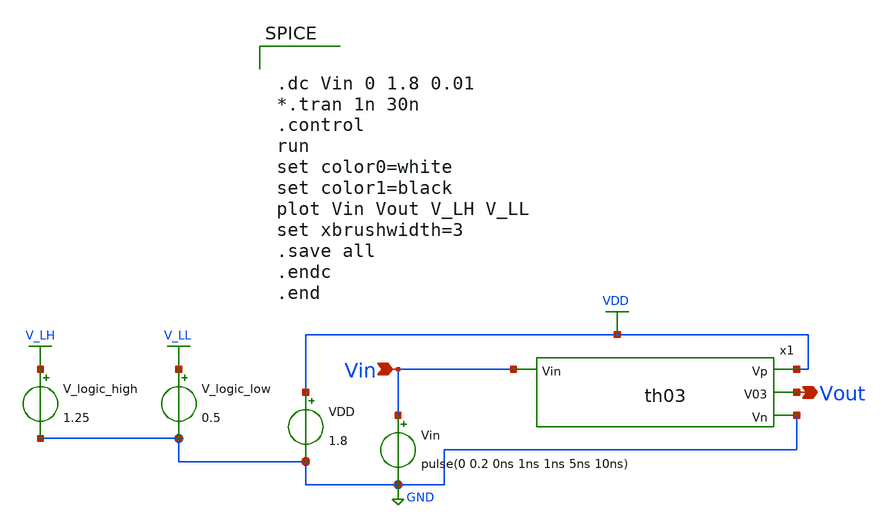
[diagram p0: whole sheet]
** sch_path: xschem/Vth_sch/Pre_layout/th03.sch
**.subckt th03 Vin Vout
*.ipin Vin
*.opin Vout
VDD VDD GND 1.8
Vin Vin GND pulse(0 0.2 0ns 1ns 1ns 5ns 10ns)
V_logic_high V_LH GND 1.25
V_logic_low V_LL GND 0.5
x1 VDD Vout Vin GND th03
**** begin user architecture code


.lib /usr/local/share/pdk/sky130A/libs.tech/ngspice/sky130.lib.spice tt

.save all





.dc Vin 0 1.8 0.01
*.tran 1n 30n
.control
run
set color0=white
set color1=black
plot Vin Vout V_LH V_LL
set xbrushwidth=3
.save all
.endc
.end


**** end user architecture code
**.ends

* expanding   symbol:  /home/exotic/Desktop/ASIC_ADC/xschem/Vth_sch/Symbol/th03.sym # of pins=4
** sym_path: xschem/Vth_sch/Symbol/th03.sym
** sch_path: xschem/Vth_sch/Symbol/th03.sch
.subckt th03 Vp V03 Vin Vn
*.opin Vn
*.opin Vp
*.ipin Vin
*.opin V03
XM3 V03 net1 Vp Vp sky130_fd_pr__pfet_01v8 L=0.156 W=1.0 nf=1 ad='int((nf+1)/2) * W/nf * 0.29' as='int((nf+2)/2) * W/nf * 0.29'
+ pd='2*int((nf+1)/2) * (W/nf + 0.29)' ps='2*int((nf+2)/2) * (W/nf + 0.29)' nrd='0.29 / W' nrs='0.29 / W'
+ sa=0 sb=0 sd=0 mult=1 m=1
XM4 V03 net1 Vn Vn sky130_fd_pr__nfet_01v8 L=1.5 W=0.40 nf=1 ad='int((nf+1)/2) * W/nf * 0.29' as='int((nf+2)/2) * W/nf * 0.29'
+ pd='2*int((nf+1)/2) * (W/nf + 0.29)' ps='2*int((nf+2)/2) * (W/nf + 0.29)' nrd='0.29 / W' nrs='0.29 / W'
+ sa=0 sb=0 sd=0 mult=1 m=1
XM1 net1 Vin net2 Vp sky130_fd_pr__pfet_01v8 L=1.36 W=0.44 nf=1 ad='int((nf+1)/2) * W/nf * 0.29' as='int((nf+2)/2) * W/nf * 0.29'
+ pd='2*int((nf+1)/2) * (W/nf + 0.29)' ps='2*int((nf+2)/2) * (W/nf + 0.29)' nrd='0.29 / W' nrs='0.29 / W'
+ sa=0 sb=0 sd=0 mult=1 m=1
XM0 net1 Vin Vn Vn sky130_fd_pr__nfet_01v8 L=0.153 W=1.1 nf=1 ad='int((nf+1)/2) * W/nf * 0.29' as='int((nf+2)/2) * W/nf * 0.29'
+ pd='2*int((nf+1)/2) * (W/nf + 0.29)' ps='2*int((nf+2)/2) * (W/nf + 0.29)' nrd='0.29 / W' nrs='0.29 / W'
+ sa=0 sb=0 sd=0 mult=1 m=1
XM2 Vp Vp net2 Vn sky130_fd_pr__nfet_01v8 L=1.5 W=0.36 nf=1 ad='int((nf+1)/2) * W/nf * 0.29' as='int((nf+2)/2) * W/nf * 0.29'
+ pd='2*int((nf+1)/2) * (W/nf + 0.29)' ps='2*int((nf+2)/2) * (W/nf + 0.29)' nrd='0.29 / W' nrs='0.29 / W'
+ sa=0 sb=0 sd=0 mult=1 m=1
.ends

.GLOBAL VDD
.GLOBAL GND
.GLOBAL V_LH
.GLOBAL V_LL
.end
